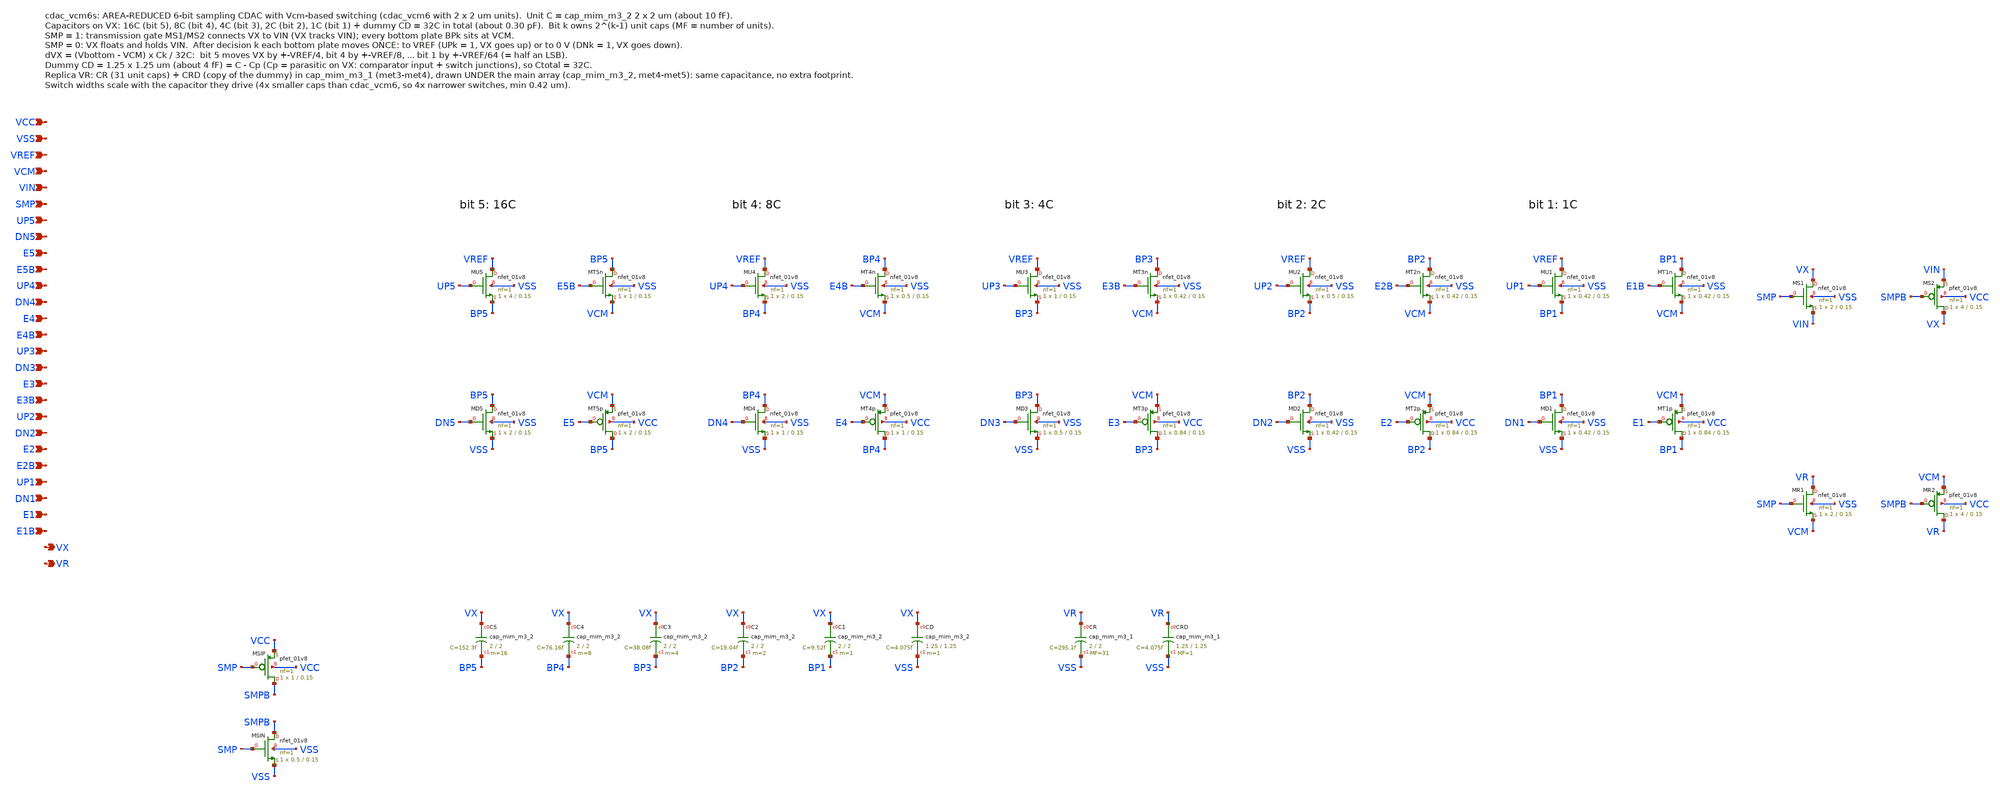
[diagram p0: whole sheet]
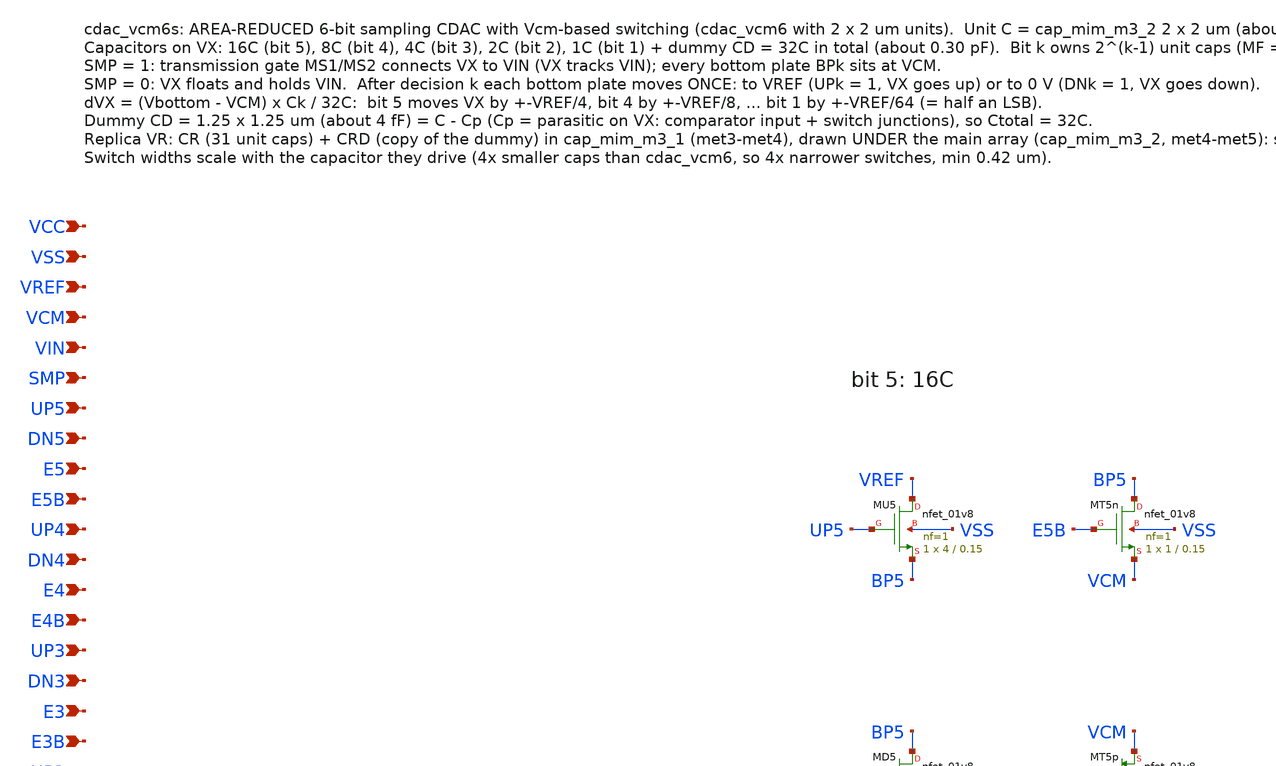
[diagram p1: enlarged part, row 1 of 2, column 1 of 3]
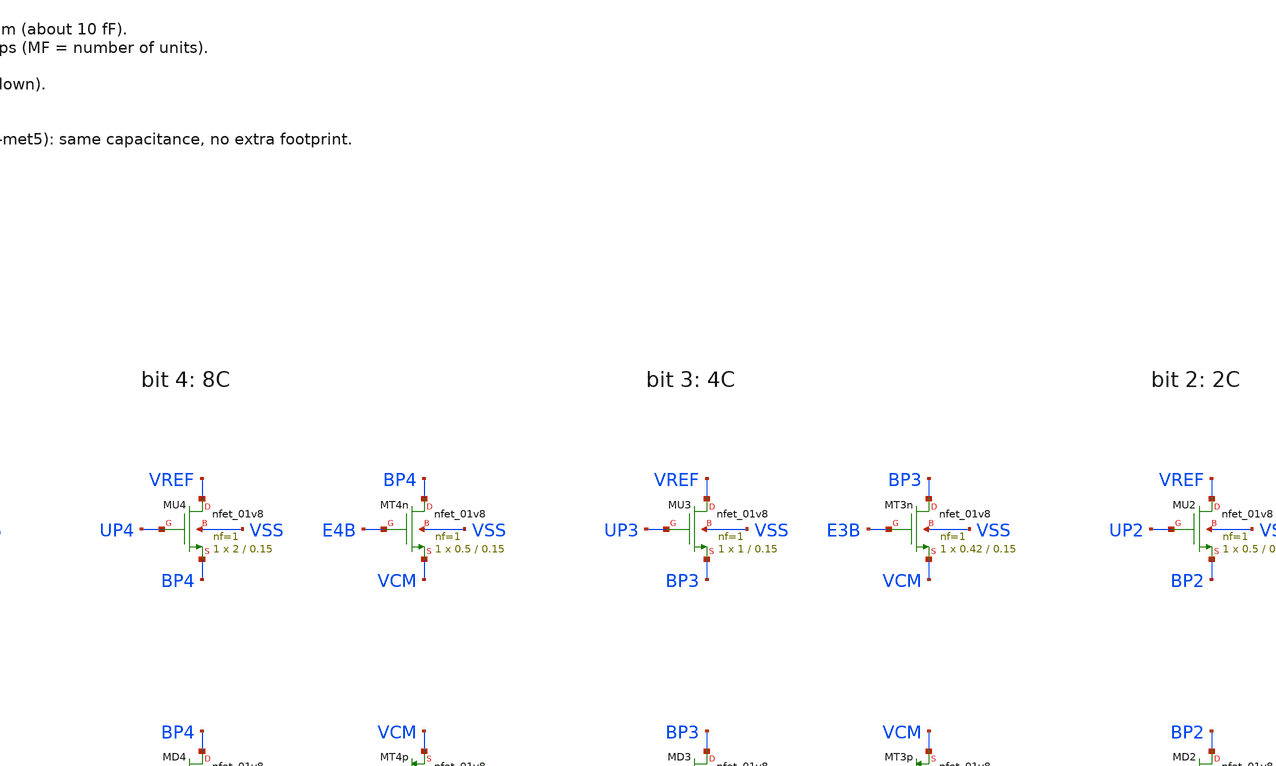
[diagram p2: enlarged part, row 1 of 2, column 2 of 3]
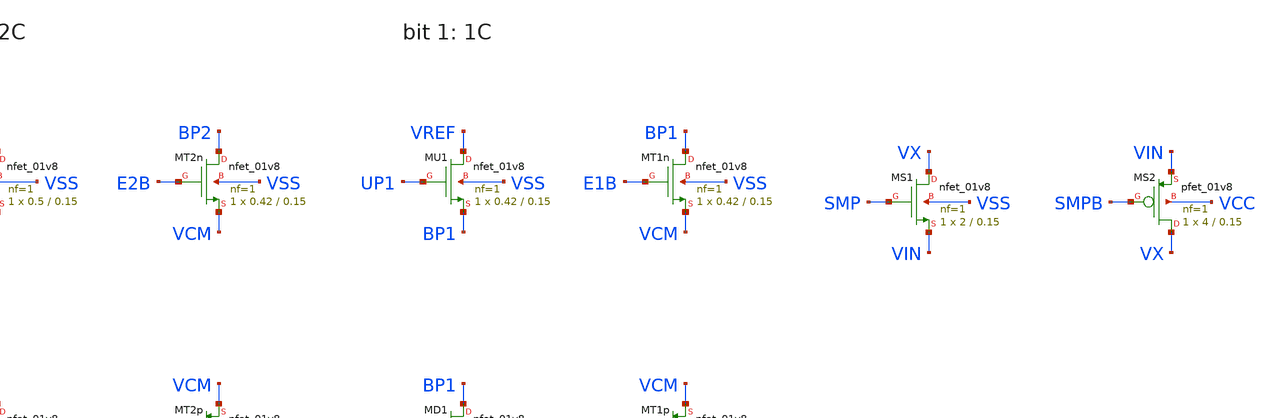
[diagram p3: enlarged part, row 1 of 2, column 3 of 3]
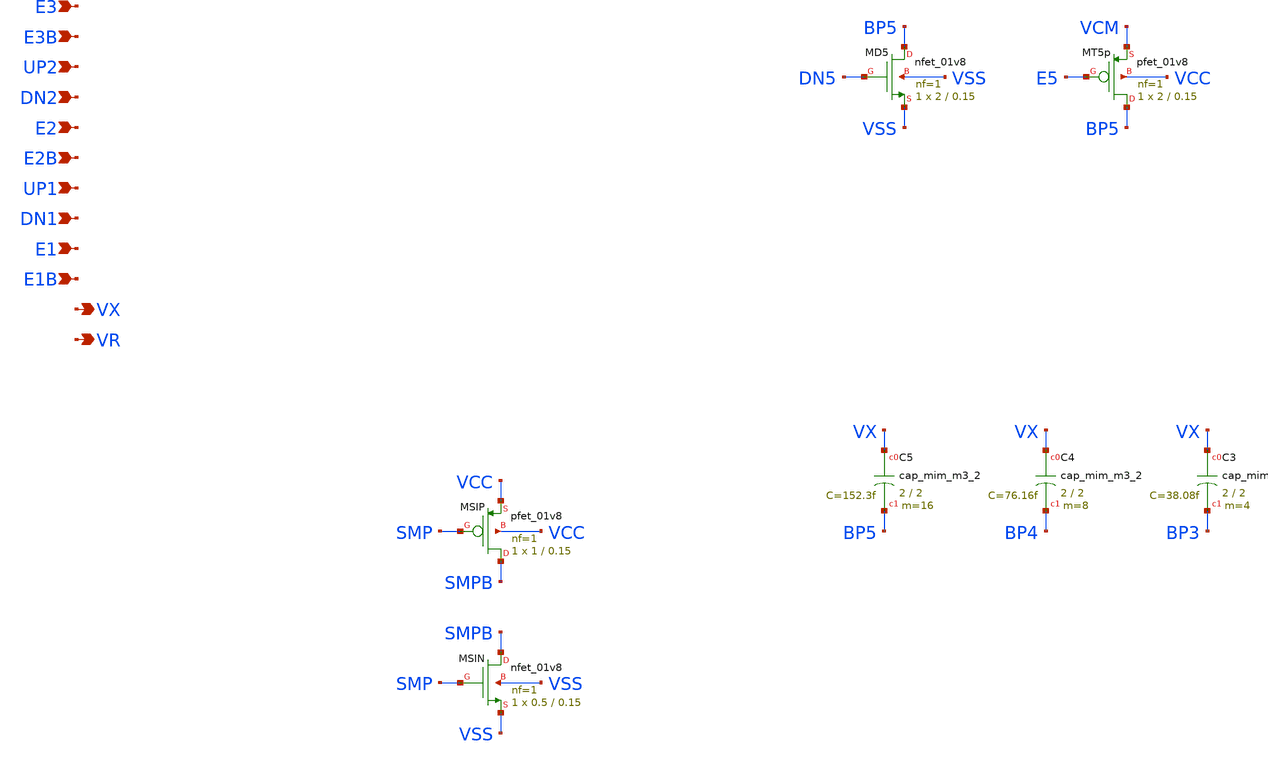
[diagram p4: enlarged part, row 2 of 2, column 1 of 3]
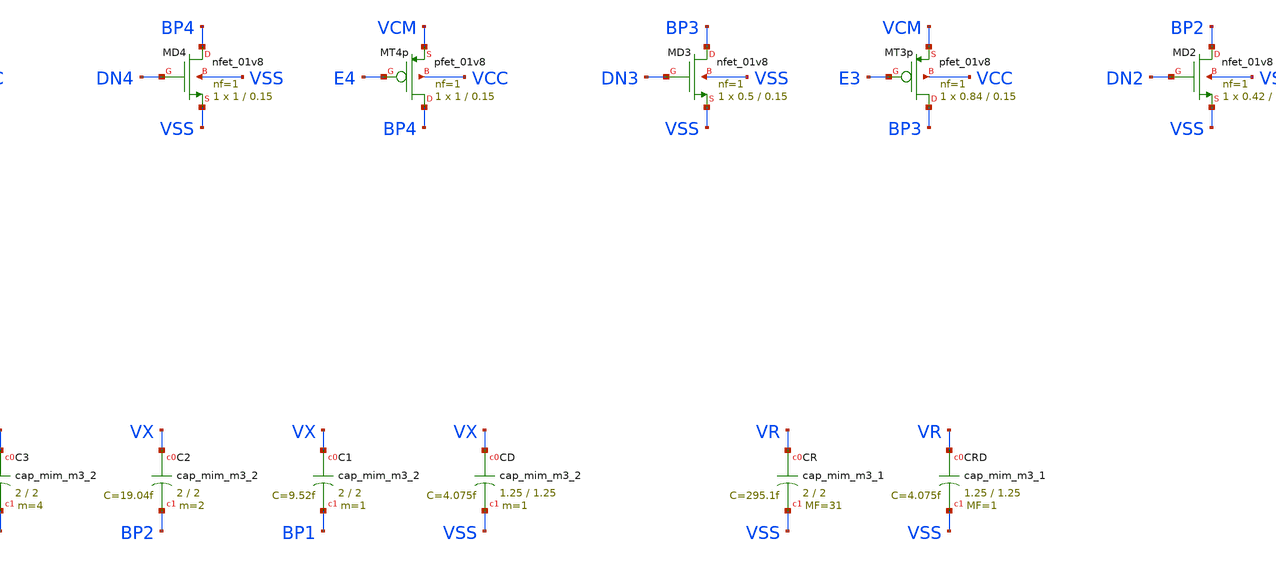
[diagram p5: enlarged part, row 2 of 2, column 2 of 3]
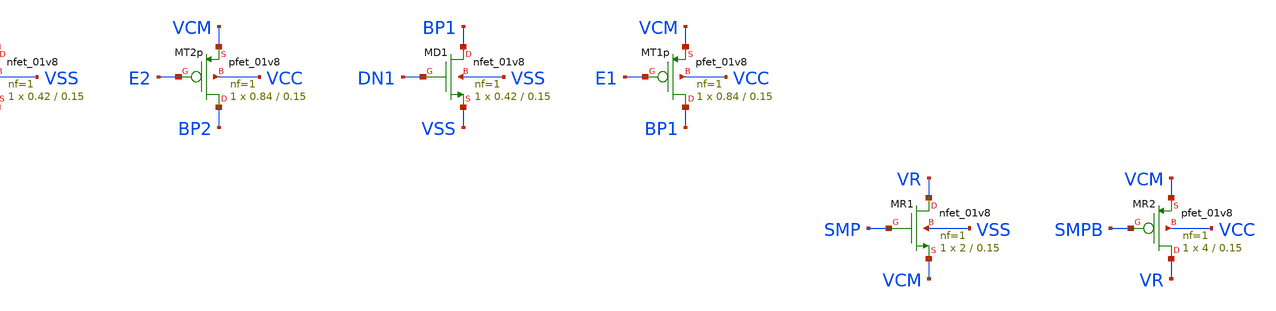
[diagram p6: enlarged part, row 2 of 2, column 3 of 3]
** sch_path: SAR_improved/cdac_vcm6s.sch
**.subckt cdac_vcm6s VCC VSS VREF VCM VIN SMP UP5 DN5 E5 E5B UP4 DN4 E4 E4B UP3 DN3 E3 E3B UP2 DN2
*+ E2 E2B UP1 DN1 E1 E1B VX VR
*.ipin VCC
*.ipin VSS
*.ipin VREF
*.ipin VCM
*.ipin VIN
*.ipin SMP
*.ipin UP5
*.ipin DN5
*.ipin E5
*.ipin E5B
*.ipin UP4
*.ipin DN4
*.ipin E4
*.ipin E4B
*.ipin UP3
*.ipin DN3
*.ipin E3
*.ipin E3B
*.ipin UP2
*.ipin DN2
*.ipin E2
*.ipin E2B
*.ipin UP1
*.ipin DN1
*.ipin E1
*.ipin E1B
*.opin VX
*.opin VR
XMS1 VX SMP VIN VSS sky130_fd_pr__nfet_01v8 L=0.15 W=2 nf=1 ad='int((nf+1)/2) * W/nf * 0.29' as='int((nf+2)/2) * W/nf * 0.29'
+ pd='2*int((nf+1)/2) * (W/nf + 0.29)' ps='2*int((nf+2)/2) * (W/nf + 0.29)' nrd='0.29 / W' nrs='0.29 / W'
+ sa=0 sb=0 sd=0 mult=1 m=1
XMS2 VX SMPB VIN VCC sky130_fd_pr__pfet_01v8 L=0.15 W=4 nf=1 ad='int((nf+1)/2) * W/nf * 0.29' as='int((nf+2)/2) * W/nf * 0.29'
+ pd='2*int((nf+1)/2) * (W/nf + 0.29)' ps='2*int((nf+2)/2) * (W/nf + 0.29)' nrd='0.29 / W' nrs='0.29 / W'
+ sa=0 sb=0 sd=0 mult=1 m=1
XMR1 VR SMP VCM VSS sky130_fd_pr__nfet_01v8 L=0.15 W=2 nf=1 ad='int((nf+1)/2) * W/nf * 0.29' as='int((nf+2)/2) * W/nf * 0.29'
+ pd='2*int((nf+1)/2) * (W/nf + 0.29)' ps='2*int((nf+2)/2) * (W/nf + 0.29)' nrd='0.29 / W' nrs='0.29 / W'
+ sa=0 sb=0 sd=0 mult=1 m=1
XMR2 VR SMPB VCM VCC sky130_fd_pr__pfet_01v8 L=0.15 W=4 nf=1 ad='int((nf+1)/2) * W/nf * 0.29' as='int((nf+2)/2) * W/nf * 0.29'
+ pd='2*int((nf+1)/2) * (W/nf + 0.29)' ps='2*int((nf+2)/2) * (W/nf + 0.29)' nrd='0.29 / W' nrs='0.29 / W'
+ sa=0 sb=0 sd=0 mult=1 m=1
XMSIP SMPB SMP VCC VCC sky130_fd_pr__pfet_01v8 L=0.15 W=1 nf=1 ad='int((nf+1)/2) * W/nf * 0.29' as='int((nf+2)/2) * W/nf * 0.29'
+ pd='2*int((nf+1)/2) * (W/nf + 0.29)' ps='2*int((nf+2)/2) * (W/nf + 0.29)' nrd='0.29 / W' nrs='0.29 / W'
+ sa=0 sb=0 sd=0 mult=1 m=1
XMSIN SMPB SMP VSS VSS sky130_fd_pr__nfet_01v8 L=0.15 W=0.5 nf=1 ad='int((nf+1)/2) * W/nf * 0.29' as='int((nf+2)/2) * W/nf * 0.29'
+ pd='2*int((nf+1)/2) * (W/nf + 0.29)' ps='2*int((nf+2)/2) * (W/nf + 0.29)' nrd='0.29 / W' nrs='0.29 / W'
+ sa=0 sb=0 sd=0 mult=1 m=1
XMU5 VREF UP5 BP5 VSS sky130_fd_pr__nfet_01v8 L=0.15 W=4 nf=1 ad='int((nf+1)/2) * W/nf * 0.29' as='int((nf+2)/2) * W/nf * 0.29'
+ pd='2*int((nf+1)/2) * (W/nf + 0.29)' ps='2*int((nf+2)/2) * (W/nf + 0.29)' nrd='0.29 / W' nrs='0.29 / W'
+ sa=0 sb=0 sd=0 mult=1 m=1
XMD5 BP5 DN5 VSS VSS sky130_fd_pr__nfet_01v8 L=0.15 W=2 nf=1 ad='int((nf+1)/2) * W/nf * 0.29' as='int((nf+2)/2) * W/nf * 0.29'
+ pd='2*int((nf+1)/2) * (W/nf + 0.29)' ps='2*int((nf+2)/2) * (W/nf + 0.29)' nrd='0.29 / W' nrs='0.29 / W'
+ sa=0 sb=0 sd=0 mult=1 m=1
XMT5n BP5 E5B VCM VSS sky130_fd_pr__nfet_01v8 L=0.15 W=1 nf=1 ad='int((nf+1)/2) * W/nf * 0.29' as='int((nf+2)/2) * W/nf * 0.29'
+ pd='2*int((nf+1)/2) * (W/nf + 0.29)' ps='2*int((nf+2)/2) * (W/nf + 0.29)' nrd='0.29 / W' nrs='0.29 / W'
+ sa=0 sb=0 sd=0 mult=1 m=1
XMT5p BP5 E5 VCM VCC sky130_fd_pr__pfet_01v8 L=0.15 W=2 nf=1 ad='int((nf+1)/2) * W/nf * 0.29' as='int((nf+2)/2) * W/nf * 0.29'
+ pd='2*int((nf+1)/2) * (W/nf + 0.29)' ps='2*int((nf+2)/2) * (W/nf + 0.29)' nrd='0.29 / W' nrs='0.29 / W'
+ sa=0 sb=0 sd=0 mult=1 m=1
XMU4 VREF UP4 BP4 VSS sky130_fd_pr__nfet_01v8 L=0.15 W=2 nf=1 ad='int((nf+1)/2) * W/nf * 0.29' as='int((nf+2)/2) * W/nf * 0.29'
+ pd='2*int((nf+1)/2) * (W/nf + 0.29)' ps='2*int((nf+2)/2) * (W/nf + 0.29)' nrd='0.29 / W' nrs='0.29 / W'
+ sa=0 sb=0 sd=0 mult=1 m=1
XMD4 BP4 DN4 VSS VSS sky130_fd_pr__nfet_01v8 L=0.15 W=1 nf=1 ad='int((nf+1)/2) * W/nf * 0.29' as='int((nf+2)/2) * W/nf * 0.29'
+ pd='2*int((nf+1)/2) * (W/nf + 0.29)' ps='2*int((nf+2)/2) * (W/nf + 0.29)' nrd='0.29 / W' nrs='0.29 / W'
+ sa=0 sb=0 sd=0 mult=1 m=1
XMT4n BP4 E4B VCM VSS sky130_fd_pr__nfet_01v8 L=0.15 W=0.5 nf=1 ad='int((nf+1)/2) * W/nf * 0.29' as='int((nf+2)/2) * W/nf * 0.29'
+ pd='2*int((nf+1)/2) * (W/nf + 0.29)' ps='2*int((nf+2)/2) * (W/nf + 0.29)' nrd='0.29 / W' nrs='0.29 / W'
+ sa=0 sb=0 sd=0 mult=1 m=1
XMT4p BP4 E4 VCM VCC sky130_fd_pr__pfet_01v8 L=0.15 W=1 nf=1 ad='int((nf+1)/2) * W/nf * 0.29' as='int((nf+2)/2) * W/nf * 0.29'
+ pd='2*int((nf+1)/2) * (W/nf + 0.29)' ps='2*int((nf+2)/2) * (W/nf + 0.29)' nrd='0.29 / W' nrs='0.29 / W'
+ sa=0 sb=0 sd=0 mult=1 m=1
XMU3 VREF UP3 BP3 VSS sky130_fd_pr__nfet_01v8 L=0.15 W=1 nf=1 ad='int((nf+1)/2) * W/nf * 0.29' as='int((nf+2)/2) * W/nf * 0.29'
+ pd='2*int((nf+1)/2) * (W/nf + 0.29)' ps='2*int((nf+2)/2) * (W/nf + 0.29)' nrd='0.29 / W' nrs='0.29 / W'
+ sa=0 sb=0 sd=0 mult=1 m=1
XMD3 BP3 DN3 VSS VSS sky130_fd_pr__nfet_01v8 L=0.15 W=0.5 nf=1 ad='int((nf+1)/2) * W/nf * 0.29' as='int((nf+2)/2) * W/nf * 0.29'
+ pd='2*int((nf+1)/2) * (W/nf + 0.29)' ps='2*int((nf+2)/2) * (W/nf + 0.29)' nrd='0.29 / W' nrs='0.29 / W'
+ sa=0 sb=0 sd=0 mult=1 m=1
XMT3n BP3 E3B VCM VSS sky130_fd_pr__nfet_01v8 L=0.15 W=0.42 nf=1 ad='int((nf+1)/2) * W/nf * 0.29' as='int((nf+2)/2) * W/nf * 0.29'
+ pd='2*int((nf+1)/2) * (W/nf + 0.29)' ps='2*int((nf+2)/2) * (W/nf + 0.29)' nrd='0.29 / W' nrs='0.29 / W'
+ sa=0 sb=0 sd=0 mult=1 m=1
XMT3p BP3 E3 VCM VCC sky130_fd_pr__pfet_01v8 L=0.15 W=0.84 nf=1 ad='int((nf+1)/2) * W/nf * 0.29' as='int((nf+2)/2) * W/nf * 0.29'
+ pd='2*int((nf+1)/2) * (W/nf + 0.29)' ps='2*int((nf+2)/2) * (W/nf + 0.29)' nrd='0.29 / W' nrs='0.29 / W'
+ sa=0 sb=0 sd=0 mult=1 m=1
XMU2 VREF UP2 BP2 VSS sky130_fd_pr__nfet_01v8 L=0.15 W=0.5 nf=1 ad='int((nf+1)/2) * W/nf * 0.29' as='int((nf+2)/2) * W/nf * 0.29'
+ pd='2*int((nf+1)/2) * (W/nf + 0.29)' ps='2*int((nf+2)/2) * (W/nf + 0.29)' nrd='0.29 / W' nrs='0.29 / W'
+ sa=0 sb=0 sd=0 mult=1 m=1
XMD2 BP2 DN2 VSS VSS sky130_fd_pr__nfet_01v8 L=0.15 W=0.42 nf=1 ad='int((nf+1)/2) * W/nf * 0.29' as='int((nf+2)/2) * W/nf * 0.29'
+ pd='2*int((nf+1)/2) * (W/nf + 0.29)' ps='2*int((nf+2)/2) * (W/nf + 0.29)' nrd='0.29 / W' nrs='0.29 / W'
+ sa=0 sb=0 sd=0 mult=1 m=1
XMT2n BP2 E2B VCM VSS sky130_fd_pr__nfet_01v8 L=0.15 W=0.42 nf=1 ad='int((nf+1)/2) * W/nf * 0.29' as='int((nf+2)/2) * W/nf * 0.29'
+ pd='2*int((nf+1)/2) * (W/nf + 0.29)' ps='2*int((nf+2)/2) * (W/nf + 0.29)' nrd='0.29 / W' nrs='0.29 / W'
+ sa=0 sb=0 sd=0 mult=1 m=1
XMT2p BP2 E2 VCM VCC sky130_fd_pr__pfet_01v8 L=0.15 W=0.84 nf=1 ad='int((nf+1)/2) * W/nf * 0.29' as='int((nf+2)/2) * W/nf * 0.29'
+ pd='2*int((nf+1)/2) * (W/nf + 0.29)' ps='2*int((nf+2)/2) * (W/nf + 0.29)' nrd='0.29 / W' nrs='0.29 / W'
+ sa=0 sb=0 sd=0 mult=1 m=1
XMU1 VREF UP1 BP1 VSS sky130_fd_pr__nfet_01v8 L=0.15 W=0.42 nf=1 ad='int((nf+1)/2) * W/nf * 0.29' as='int((nf+2)/2) * W/nf * 0.29'
+ pd='2*int((nf+1)/2) * (W/nf + 0.29)' ps='2*int((nf+2)/2) * (W/nf + 0.29)' nrd='0.29 / W' nrs='0.29 / W'
+ sa=0 sb=0 sd=0 mult=1 m=1
XMD1 BP1 DN1 VSS VSS sky130_fd_pr__nfet_01v8 L=0.15 W=0.42 nf=1 ad='int((nf+1)/2) * W/nf * 0.29' as='int((nf+2)/2) * W/nf * 0.29'
+ pd='2*int((nf+1)/2) * (W/nf + 0.29)' ps='2*int((nf+2)/2) * (W/nf + 0.29)' nrd='0.29 / W' nrs='0.29 / W'
+ sa=0 sb=0 sd=0 mult=1 m=1
XMT1n BP1 E1B VCM VSS sky130_fd_pr__nfet_01v8 L=0.15 W=0.42 nf=1 ad='int((nf+1)/2) * W/nf * 0.29' as='int((nf+2)/2) * W/nf * 0.29'
+ pd='2*int((nf+1)/2) * (W/nf + 0.29)' ps='2*int((nf+2)/2) * (W/nf + 0.29)' nrd='0.29 / W' nrs='0.29 / W'
+ sa=0 sb=0 sd=0 mult=1 m=1
XMT1p BP1 E1 VCM VCC sky130_fd_pr__pfet_01v8 L=0.15 W=0.84 nf=1 ad='int((nf+1)/2) * W/nf * 0.29' as='int((nf+2)/2) * W/nf * 0.29'
+ pd='2*int((nf+1)/2) * (W/nf + 0.29)' ps='2*int((nf+2)/2) * (W/nf + 0.29)' nrd='0.29 / W' nrs='0.29 / W'
+ sa=0 sb=0 sd=0 mult=1 m=1
XC5 VX BP5 sky130_fd_pr__cap_mim_m3_2 W=2 L=2 MF=16 m=16
XC4 VX BP4 sky130_fd_pr__cap_mim_m3_2 W=2 L=2 MF=8 m=8
XC3 VX BP3 sky130_fd_pr__cap_mim_m3_2 W=2 L=2 MF=4 m=4
XC2 VX BP2 sky130_fd_pr__cap_mim_m3_2 W=2 L=2 MF=2 m=2
XC1 VX BP1 sky130_fd_pr__cap_mim_m3_2 W=2 L=2 MF=1 m=1
XCD VX VSS sky130_fd_pr__cap_mim_m3_2 W=1.25 L=1.25 MF=1 m=1
XCR VR VSS sky130_fd_pr__cap_mim_m3_1 W=2 L=2 MF=31 m=31
XCRD VR VSS sky130_fd_pr__cap_mim_m3_1 W=1.25 L=1.25 MF=1 m=1
**.ends
.end
